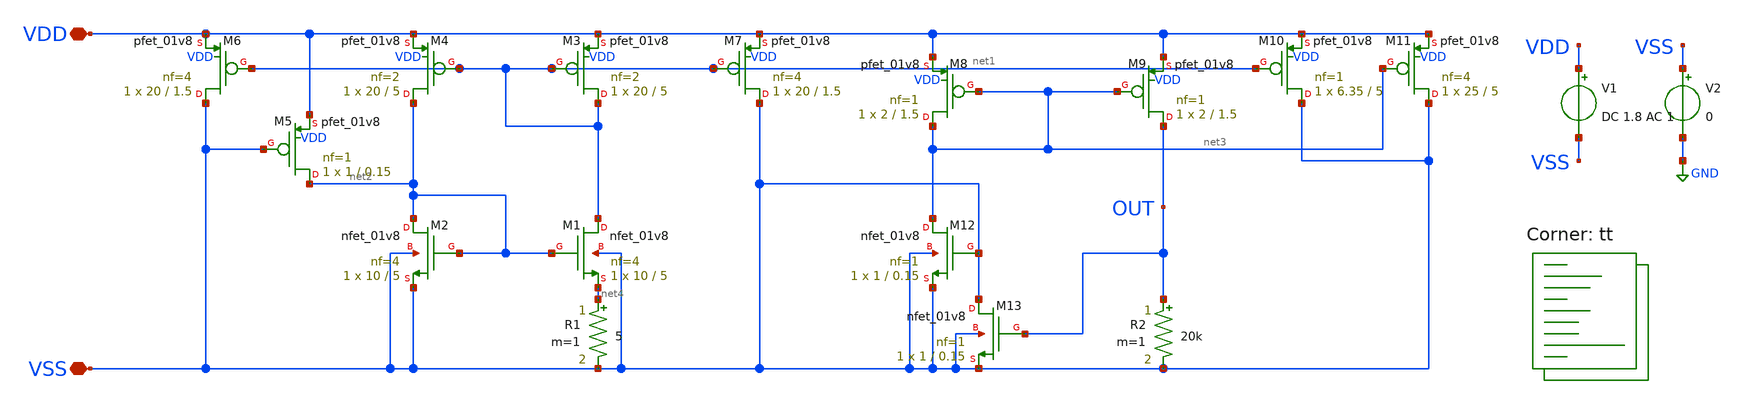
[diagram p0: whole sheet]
** sch_path: bandgap/current-ref/current-bandgap.sch
**.subckt current-bandgap VDD VSS
*.iopin VDD
*.iopin VSS
XM1 net1 net2 net4 VSS sky130_fd_pr__nfet_01v8 L=5 W=10 nf=4 ad='int((nf+1)/2) * W/nf * 0.29' as='int((nf+2)/2) * W/nf * 0.29'
+ pd='2*int((nf+1)/2) * (W/nf + 0.29)' ps='2*int((nf+2)/2) * (W/nf + 0.29)' nrd='0.29 / W' nrs='0.29 / W'
+ sa=0 sb=0 sd=0 mult=1 m=1
XM2 net2 net2 VSS VSS sky130_fd_pr__nfet_01v8 L=5 W=10 nf=4 ad='int((nf+1)/2) * W/nf * 0.29' as='int((nf+2)/2) * W/nf * 0.29'
+ pd='2*int((nf+1)/2) * (W/nf + 0.29)' ps='2*int((nf+2)/2) * (W/nf + 0.29)' nrd='0.29 / W' nrs='0.29 / W'
+ sa=0 sb=0 sd=0 mult=1 m=1
XM3 net1 net1 VDD VDD sky130_fd_pr__pfet_01v8 L=5 W=20 nf=2 ad='int((nf+1)/2) * W/nf * 0.29' as='int((nf+2)/2) * W/nf * 0.29'
+ pd='2*int((nf+1)/2) * (W/nf + 0.29)' ps='2*int((nf+2)/2) * (W/nf + 0.29)' nrd='0.29 / W' nrs='0.29 / W'
+ sa=0 sb=0 sd=0 mult=1 m=1
XM4 net2 net1 VDD VDD sky130_fd_pr__pfet_01v8 L=5 W=20 nf=2 ad='int((nf+1)/2) * W/nf * 0.29' as='int((nf+2)/2) * W/nf * 0.29'
+ pd='2*int((nf+1)/2) * (W/nf + 0.29)' ps='2*int((nf+2)/2) * (W/nf + 0.29)' nrd='0.29 / W' nrs='0.29 / W'
+ sa=0 sb=0 sd=0 mult=1 m=1
XM5 net2 VSS VDD VDD sky130_fd_pr__pfet_01v8 L=0.15 W=1 nf=1 ad='int((nf+1)/2) * W/nf * 0.29' as='int((nf+2)/2) * W/nf * 0.29'
+ pd='2*int((nf+1)/2) * (W/nf + 0.29)' ps='2*int((nf+2)/2) * (W/nf + 0.29)' nrd='0.29 / W' nrs='0.29 / W'
+ sa=0 sb=0 sd=0 mult=1 m=1
XM6 VSS net1 VDD VDD sky130_fd_pr__pfet_01v8 L=1.5 W=20 nf=4 ad='int((nf+1)/2) * W/nf * 0.29' as='int((nf+2)/2) * W/nf * 0.29'
+ pd='2*int((nf+1)/2) * (W/nf + 0.29)' ps='2*int((nf+2)/2) * (W/nf + 0.29)' nrd='0.29 / W' nrs='0.29 / W'
+ sa=0 sb=0 sd=0 mult=1 m=1
XM7 VSS net1 VDD VDD sky130_fd_pr__pfet_01v8 L=1.5 W=20 nf=4 ad='int((nf+1)/2) * W/nf * 0.29' as='int((nf+2)/2) * W/nf * 0.29'
+ pd='2*int((nf+1)/2) * (W/nf + 0.29)' ps='2*int((nf+2)/2) * (W/nf + 0.29)' nrd='0.29 / W' nrs='0.29 / W'
+ sa=0 sb=0 sd=0 mult=1 m=1
XM8 net3 net3 VDD VDD sky130_fd_pr__pfet_01v8 L=1.5 W=2 nf=1 ad='int((nf+1)/2) * W/nf * 0.29' as='int((nf+2)/2) * W/nf * 0.29'
+ pd='2*int((nf+1)/2) * (W/nf + 0.29)' ps='2*int((nf+2)/2) * (W/nf + 0.29)' nrd='0.29 / W' nrs='0.29 / W'
+ sa=0 sb=0 sd=0 mult=1 m=1
XM9 OUT net3 VDD VDD sky130_fd_pr__pfet_01v8 L=1.5 W=2 nf=1 ad='int((nf+1)/2) * W/nf * 0.29' as='int((nf+2)/2) * W/nf * 0.29'
+ pd='2*int((nf+1)/2) * (W/nf + 0.29)' ps='2*int((nf+2)/2) * (W/nf + 0.29)' nrd='0.29 / W' nrs='0.29 / W'
+ sa=0 sb=0 sd=0 mult=1 m=1
XM10 VSS net1 VDD VDD sky130_fd_pr__pfet_01v8 L=5 W=6.35 nf=1 ad='int((nf+1)/2) * W/nf * 0.29' as='int((nf+2)/2) * W/nf * 0.29'
+ pd='2*int((nf+1)/2) * (W/nf + 0.29)' ps='2*int((nf+2)/2) * (W/nf + 0.29)' nrd='0.29 / W' nrs='0.29 / W'
+ sa=0 sb=0 sd=0 mult=1 m=1
XM11 VSS net3 VDD VDD sky130_fd_pr__pfet_01v8 L=5 W=25 nf=4 ad='int((nf+1)/2) * W/nf * 0.29' as='int((nf+2)/2) * W/nf * 0.29'
+ pd='2*int((nf+1)/2) * (W/nf + 0.29)' ps='2*int((nf+2)/2) * (W/nf + 0.29)' nrd='0.29 / W' nrs='0.29 / W'
+ sa=0 sb=0 sd=0 mult=1 m=1
XM12 net3 VSS VSS VSS sky130_fd_pr__nfet_01v8 L=0.15 W=1 nf=1 ad='int((nf+1)/2) * W/nf * 0.29' as='int((nf+2)/2) * W/nf * 0.29'
+ pd='2*int((nf+1)/2) * (W/nf + 0.29)' ps='2*int((nf+2)/2) * (W/nf + 0.29)' nrd='0.29 / W' nrs='0.29 / W'
+ sa=0 sb=0 sd=0 mult=1 m=1
XM13 VSS OUT VSS VSS sky130_fd_pr__nfet_01v8 L=0.15 W=1 nf=1 ad='int((nf+1)/2) * W/nf * 0.29' as='int((nf+2)/2) * W/nf * 0.29'
+ pd='2*int((nf+1)/2) * (W/nf + 0.29)' ps='2*int((nf+2)/2) * (W/nf + 0.29)' nrd='0.29 / W' nrs='0.29 / W'
+ sa=0 sb=0 sd=0 mult=1 m=1
R1 net4 VSS 5 m=1
R2 OUT VSS 20k m=1
V1 VDD VSS DC 1.8 AC 1
V2 VSS GND 0
**** begin user architecture code
.lib $::SKYWATER_MODELS/sky130.lib.spice tt



.include /foss/designs/afe-icdec-teknofest-2026/bandgap/bgr/layout/current-mode-bgr_pex.spice

.control

ac dec 100 1 100T
plot -20*log10(v(OUT))

.endc


**** end user architecture code
**.ends
.GLOBAL GND
.end
